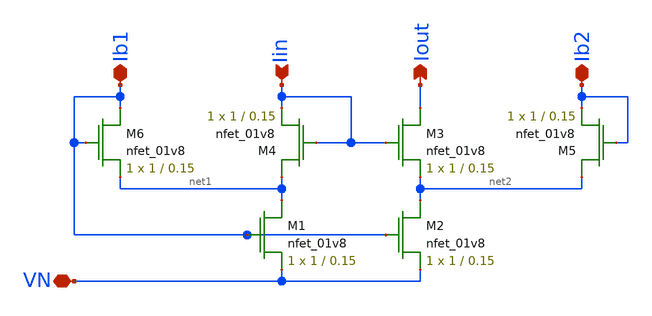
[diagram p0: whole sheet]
** sch_path: dac/schematics/low_voltage_cascode_current_mirror.sch
**.subckt low_voltage_cascode_current_mirror Ib1 Ib2 Iin Iout VN
*.iopin Ib1
*.iopin Ib2
*.ipin Iin
*.opin Iout
*.iopin VN
XM1 net1 Ib1 VN GND sky130_fd_pr__nfet_01v8 L=0.15 W=1 nf=1 ad='int((nf+1)/2) * W/nf * 0.29' as='int((nf+2)/2) * W/nf * 0.29'
+ pd='2*int((nf+1)/2) * (W/nf + 0.29)' ps='2*int((nf+2)/2) * (W/nf + 0.29)' nrd='0.29 / W' nrs='0.29 / W'
+ sa=0 sb=0 sd=0 mult=1 m=1
XM2 net2 Ib1 VN GND sky130_fd_pr__nfet_01v8 L=0.15 W=1 nf=1 ad='int((nf+1)/2) * W/nf * 0.29' as='int((nf+2)/2) * W/nf * 0.29'
+ pd='2*int((nf+1)/2) * (W/nf + 0.29)' ps='2*int((nf+2)/2) * (W/nf + 0.29)' nrd='0.29 / W' nrs='0.29 / W'
+ sa=0 sb=0 sd=0 mult=1 m=1
XM3 Iout Iin net2 GND sky130_fd_pr__nfet_01v8 L=0.15 W=1 nf=1 ad='int((nf+1)/2) * W/nf * 0.29' as='int((nf+2)/2) * W/nf * 0.29'
+ pd='2*int((nf+1)/2) * (W/nf + 0.29)' ps='2*int((nf+2)/2) * (W/nf + 0.29)' nrd='0.29 / W' nrs='0.29 / W'
+ sa=0 sb=0 sd=0 mult=1 m=1
XM4 net1 Iin Iin GND sky130_fd_pr__nfet_01v8 L=0.15 W=1 nf=1 ad='int((nf+1)/2) * W/nf * 0.29' as='int((nf+2)/2) * W/nf * 0.29'
+ pd='2*int((nf+1)/2) * (W/nf + 0.29)' ps='2*int((nf+2)/2) * (W/nf + 0.29)' nrd='0.29 / W' nrs='0.29 / W'
+ sa=0 sb=0 sd=0 mult=1 m=1
XM5 net2 Ib2 Ib2 GND sky130_fd_pr__nfet_01v8 L=0.15 W=1 nf=1 ad='int((nf+1)/2) * W/nf * 0.29' as='int((nf+2)/2) * W/nf * 0.29'
+ pd='2*int((nf+1)/2) * (W/nf + 0.29)' ps='2*int((nf+2)/2) * (W/nf + 0.29)' nrd='0.29 / W' nrs='0.29 / W'
+ sa=0 sb=0 sd=0 mult=1 m=1
XM6 Ib1 Ib1 net1 GND sky130_fd_pr__nfet_01v8 L=0.15 W=1 nf=1 ad='int((nf+1)/2) * W/nf * 0.29' as='int((nf+2)/2) * W/nf * 0.29'
+ pd='2*int((nf+1)/2) * (W/nf + 0.29)' ps='2*int((nf+2)/2) * (W/nf + 0.29)' nrd='0.29 / W' nrs='0.29 / W'
+ sa=0 sb=0 sd=0 mult=1 m=1
**.ends
.end
